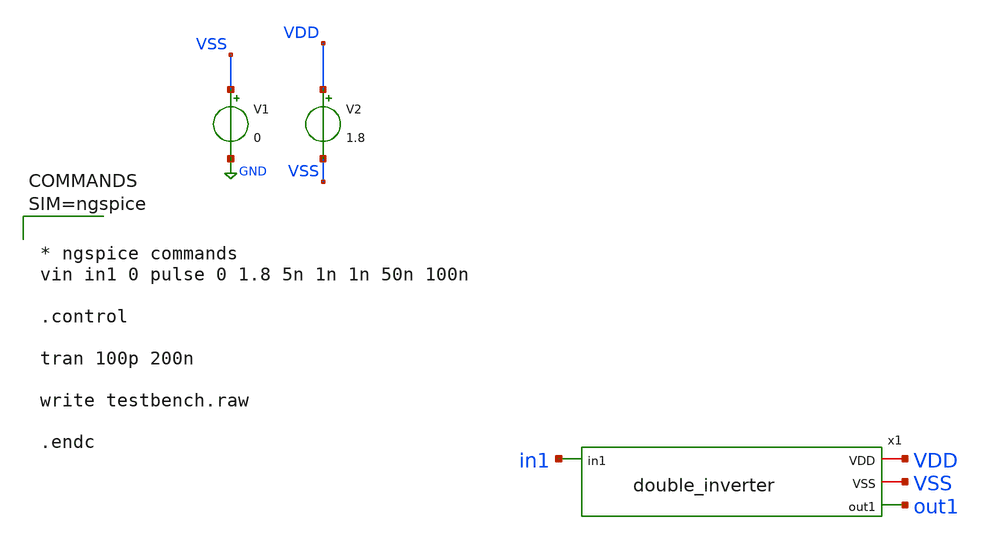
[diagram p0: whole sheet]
** sch_path: xschem/testbench.sch
**.subckt testbench
x1 VDD VSS out1 in1 double_inverter
V1 VSS GND 0
V2 VDD VSS 1.8
**** begin user architecture code

** opencircuitdesign pdks install
.lib $::SKYWATER_MODELS/sky130.lib.spice tt





* ngspice commands
vin in1 0 pulse 0 1.8 5n 1n 1n 50n 100n

.control

tran 100p 200n

write testbench.raw

.endc




**** end user architecture code
**.ends

* expanding   symbol:  double_inverter.sym # of pins=4
** sym_path: xschem/double_inverter.sym
** sch_path: xschem/double_inverter.sch
.subckt double_inverter VDD VSS out1 in1
*.iopin VDD
*.iopin VSS
*.ipin in1
*.opin out1
XM1 inverted in1 VDD VDD sky130_fd_pr__pfet_01v8 L=0.15 W=1 nf=1 ad='int((nf+1)/2) * W/nf * 0.29' as='int((nf+2)/2) * W/nf * 0.29'
+ pd='2*int((nf+1)/2) * (W/nf + 0.29)' ps='2*int((nf+2)/2) * (W/nf + 0.29)' nrd='0.29 / W' nrs='0.29 / W'
+ sa=0 sb=0 sd=0 mult=1 m=1
XM2 inverted in1 VSS VSS sky130_fd_pr__nfet_01v8 L=0.15 W=1 nf=1 ad='int((nf+1)/2) * W/nf * 0.29' as='int((nf+2)/2) * W/nf * 0.29'
+ pd='2*int((nf+1)/2) * (W/nf + 0.29)' ps='2*int((nf+2)/2) * (W/nf + 0.29)' nrd='0.29 / W' nrs='0.29 / W'
+ sa=0 sb=0 sd=0 mult=1 m=1
XM3 out1 inverted VDD VDD sky130_fd_pr__pfet_01v8 L=0.15 W=20 nf=20 ad='int((nf+1)/2) * W/nf * 0.29'
+ as='int((nf+2)/2) * W/nf * 0.29' pd='2*int((nf+1)/2) * (W/nf + 0.29)' ps='2*int((nf+2)/2) * (W/nf + 0.29)'
+ nrd='0.29 / W' nrs='0.29 / W' sa=0 sb=0 sd=0 mult=1 m=1
XM4 out1 inverted VSS VSS sky130_fd_pr__nfet_01v8 L=0.15 W=20 nf=20 ad='int((nf+1)/2) * W/nf * 0.29'
+ as='int((nf+2)/2) * W/nf * 0.29' pd='2*int((nf+1)/2) * (W/nf + 0.29)' ps='2*int((nf+2)/2) * (W/nf + 0.29)'
+ nrd='0.29 / W' nrs='0.29 / W' sa=0 sb=0 sd=0 mult=1 m=1
.ends

.GLOBAL GND
.end
